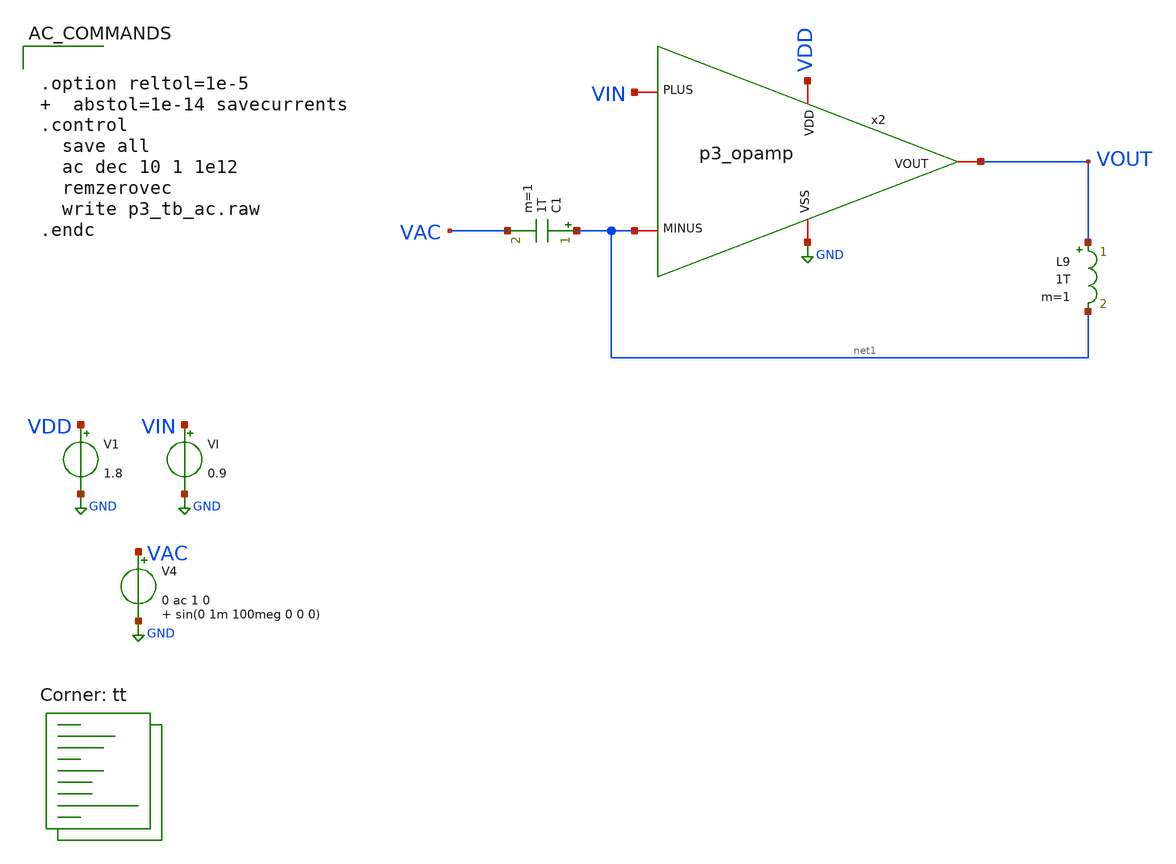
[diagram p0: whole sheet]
** sch_path: xschem/tb_p3_ac.sch
**.subckt tb_p3_ac
V1 VDD GND 1.8
VI VIN GND 0.9
V4 VAC GND 0 ac 1 0 sin(0 1m 100meg 0 0 0)
C1 net1 VAC 1T m=1
L9 VOUT net1 1T m=1
x2 VDD net1 VIN VOUT GND p3_opamp
**** begin user architecture code
.lib $::SKYWATER_MODELS/sky130.lib.spice tt


.option reltol=1e-5   abstol=1e-14 savecurrents
.control
  save all
  ac dec 10 1 1e12
  remzerovec
  write p3_tb_ac.raw
.endc


**** end user architecture code
**.ends

* expanding   symbol:  p3_opamp.sym # of pins=5
** sym_path: p3_opamp.sym
** sch_path: p3_opamp.sch
.subckt p3_opamp VDD MINUS PLUS VOUT VSS
*.iopin VDD
*.iopin VSS
*.iopin PLUS
*.iopin MINUS
*.iopin VOUT
XM3 VX VBIAS VSS VSS sky130_fd_pr__nfet_01v8 L=2 W=4 nf=4 ad='int((nf+1)/2) * W/nf * 0.29' as='int((nf+2)/2) * W/nf * 0.29'
+ pd='2*int((nf+1)/2) * (W/nf + 0.29)' ps='2*int((nf+2)/2) * (W/nf + 0.29)' nrd='0.29 / W' nrs='0.29 / W'
+ sa=0 sb=0 sd=0 mult=1 m=1
XM6 VBIAS VBIAS VSS VSS sky130_fd_pr__nfet_01v8 L=2 W=4 nf=4 ad='int((nf+1)/2) * W/nf * 0.29' as='int((nf+2)/2) * W/nf * 0.29'
+ pd='2*int((nf+1)/2) * (W/nf + 0.29)' ps='2*int((nf+2)/2) * (W/nf + 0.29)' nrd='0.29 / W' nrs='0.29 / W'
+ sa=0 sb=0 sd=0 mult=1 m=1
XM7 VOUT VBIAS VSS VSS sky130_fd_pr__nfet_01v8 L=2 W=7 nf=7 ad='int((nf+1)/2) * W/nf * 0.29' as='int((nf+2)/2) * W/nf * 0.29'
+ pd='2*int((nf+1)/2) * (W/nf + 0.29)' ps='2*int((nf+2)/2) * (W/nf + 0.29)' nrd='0.29 / W' nrs='0.29 / W'
+ sa=0 sb=0 sd=0 mult=1 m=1
XR1 VBIAS VDD VSS sky130_fd_pr__res_xhigh_po_0p35 L=2.9 mult=1 m=1
XM2 V2 MINUS VX VSS sky130_fd_pr__nfet_01v8_lvt L=0.5 W=2.5 nf=1 ad='int((nf+1)/2) * W/nf * 0.29' as='int((nf+2)/2) * W/nf * 0.29'
+ pd='2*int((nf+1)/2) * (W/nf + 0.29)' ps='2*int((nf+2)/2) * (W/nf + 0.29)' nrd='0.29 / W' nrs='0.29 / W'
+ sa=0 sb=0 sd=0 mult=1 m=1
XM1 V1 PLUS VX VSS sky130_fd_pr__nfet_01v8_lvt L=0.5 W=2.5 nf=1 ad='int((nf+1)/2) * W/nf * 0.29' as='int((nf+2)/2) * W/nf * 0.29'
+ pd='2*int((nf+1)/2) * (W/nf + 0.29)' ps='2*int((nf+2)/2) * (W/nf + 0.29)' nrd='0.29 / W' nrs='0.29 / W'
+ sa=0 sb=0 sd=0 mult=1 m=1
XM4 V2 V2 VDD VDD sky130_fd_pr__pfet_01v8_lvt L=2 W=6 nf=6 ad='int((nf+1)/2) * W/nf * 0.29' as='int((nf+2)/2) * W/nf * 0.29'
+ pd='2*int((nf+1)/2) * (W/nf + 0.29)' ps='2*int((nf+2)/2) * (W/nf + 0.29)' nrd='0.29 / W' nrs='0.29 / W'
+ sa=0 sb=0 sd=0 mult=1 m=1
XM5 V1 V2 VDD VDD sky130_fd_pr__pfet_01v8_lvt L=2 W=6 nf=6 ad='int((nf+1)/2) * W/nf * 0.29' as='int((nf+2)/2) * W/nf * 0.29'
+ pd='2*int((nf+1)/2) * (W/nf + 0.29)' ps='2*int((nf+2)/2) * (W/nf + 0.29)' nrd='0.29 / W' nrs='0.29 / W'
+ sa=0 sb=0 sd=0 mult=1 m=1
XM8 VOUT V1 VDD VDD sky130_fd_pr__pfet_01v8_lvt L=0.5 W=20 nf=20 ad='int((nf+1)/2) * W/nf * 0.29' as='int((nf+2)/2) * W/nf * 0.29'
+ pd='2*int((nf+1)/2) * (W/nf + 0.29)' ps='2*int((nf+2)/2) * (W/nf + 0.29)' nrd='0.29 / W' nrs='0.29 / W'
+ sa=0 sb=0 sd=0 mult=1 m=1
.ends

.GLOBAL GND
.end
